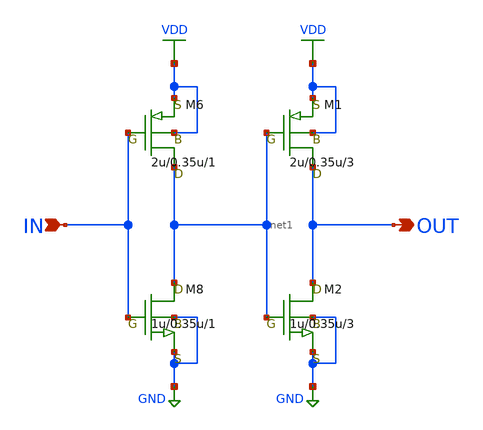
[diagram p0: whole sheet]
** sch_path: LR_hasegawa/LR_Work2/symbol/INVERTER13.sch
**.subckt INVERTER13 OUT IN
*.opin OUT
*.ipin IN
M6 net1 IN VDD VDD pch w=2u l=0.35u as=5.6p ps=9u ad=5.6p pd=9u m=1
M8 net1 IN GND GND nch w=1u l=0.35u as=2.8p ps=5.5u ad=2.8p pd=5.5u m=1
M1 OUT net1 VDD VDD pch w=2u l=0.35u as=5.6p ps=9u ad=5.6p pd=9u m=3
M2 OUT net1 GND GND nch w=1u l=0.35u as=2.8p ps=5.5u ad=2.8p pd=5.5u m=3
**.ends
.GLOBAL VDD
.GLOBAL GND
.end
